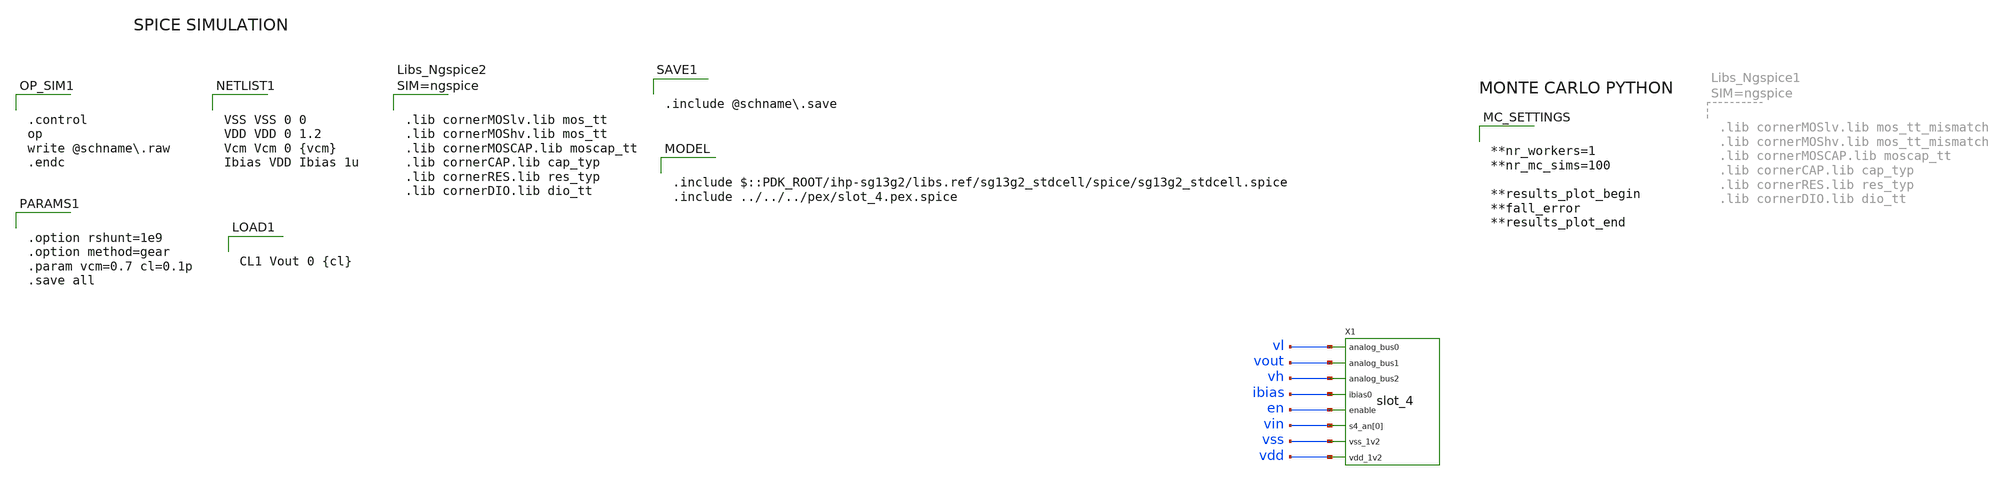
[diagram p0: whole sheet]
** sch_path: schematic/xschem/wind_comp/wind_comp_pex_tb.sch

.include $::PDK_ROOT/ihp-sg13g2/libs.ref/sg13g2_stdcell/spice/sg13g2_stdcell.spice
.include ../../../pex/slot_4.pex.spice

**.subckt wind_comp_pex_tb
X1 vl vout vh ibias en vin vss vdd slot_4
**** begin user architecture code


**nr_workers=1
**nr_mc_sims=100

**results_plot_begin
**fall_error
**results_plot_end




VSS VSS 0 0
VDD VDD 0 1.2
Vcm Vcm 0 {vcm}
Ibias VDD Ibias 1u



.control
op
write @schname.raw
.endc




.lib cornerMOSlv.lib mos_tt
.lib cornerMOShv.lib mos_tt
.lib cornerMOSCAP.lib moscap_tt
.lib cornerCAP.lib cap_typ
.lib cornerRES.lib res_typ
.lib cornerDIO.lib dio_tt





.option rshunt=1e9
.option method=gear
.param vcm=0.7 cl=0.1p
.save all




CL1 Vout 0 {cl}



.include @schname.save



Vh vh vss {vcm+0.3}
Vl vl vss {vcm-0.3}
vin vin vss sin({vcm} 0.4 1000)
ven en vss 1.2
.control
tran 100n 1m
*plot vout vh vl vin vout1
plot vout vh vl vin
meas tran fall_time find time when vin=vh fall=1
meas tran delay find time when vout={vcm} fall=1
let fall_error = delay-fall_time
echo results_save_begin
print fall_error
echo results_save_end
.endc


**** end user architecture code
**.ends
.end
